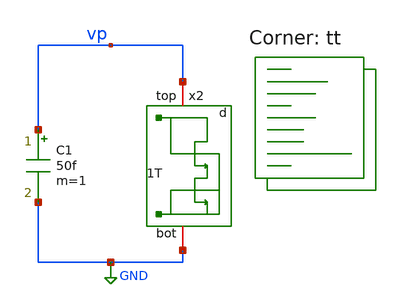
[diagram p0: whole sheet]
** sch_path: xschem/tb/dschr_nwk_type_d_tb.sch
**.subckt dschr_nwk_type_d_tb
C1 vp GND 50f m=1
x2 vp GND dschr_nwk_type_d L=0.18 W=1
**** begin user architecture code
.lib $::SKYWATER_MODELS/sky130.lib.spice tt


.include $::netlist_dir/ctrl_sims.spice


**** end user architecture code
**.ends

* expanding   symbol:  dschr_nwks/dschr_nwk_type_d.sym # of pins=2
** sym_path: xschem/dschr_nwks/dschr_nwk_type_d.sym
** sch_path: xschem/dschr_nwks/dschr_nwk_type_d.sch
.subckt dschr_nwk_type_d top bot  L=0.18 W=1
*.iopin top
*.iopin bot
XM1 top top net1 bot sky130_fd_pr__nfet_01v8 L='L' W='W' nf=1 ad='int((nf+1)/2) * W/nf * 0.29' as='int((nf+2)/2) * W/nf * 0.29'
+ pd='2*int((nf+1)/2) * (W/nf + 0.29)' ps='2*int((nf+2)/2) * (W/nf + 0.29)' nrd='0.29 / W' nrs='0.29 / W'
+ sa=0 sb=0 sd=0 mult=1 m=1
XM2 net1 bot bot bot sky130_fd_pr__nfet_01v8 L='L' W='W' nf=1 ad='int((nf+1)/2) * W/nf * 0.29' as='int((nf+2)/2) * W/nf * 0.29'
+ pd='2*int((nf+1)/2) * (W/nf + 0.29)' ps='2*int((nf+2)/2) * (W/nf + 0.29)' nrd='0.29 / W' nrs='0.29 / W'
+ sa=0 sb=0 sd=0 mult=1 m=1
.ends

.GLOBAL GND
.end
